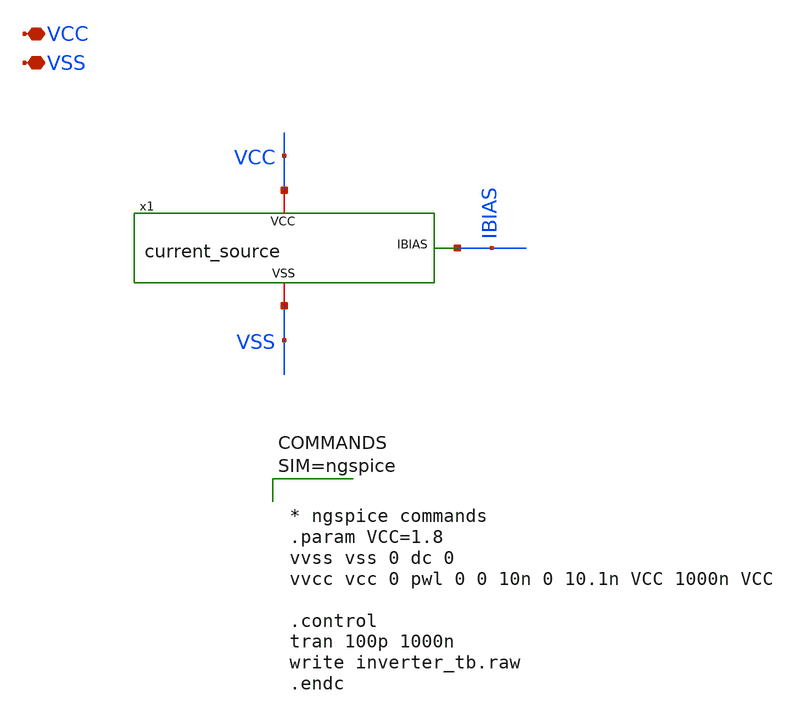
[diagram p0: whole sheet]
** sch_path: xschem/current_source_tb.sch
**.subckt current_source_tb VCC VSS
*.iopin VCC
*.iopin VSS
x1 VCC VSS IBIAS current_source
**** begin user architecture code

** opencircuitdesign pdks install
.lib $::SKYWATER_MODELS/sky130.lib.spice tt





* ngspice commands
.param VCC=1.8
vvss vss 0 dc 0
vvcc vcc 0 pwl 0 0 10n 0 10.1n VCC 1000n VCC

.control
tran 100p 1000n
write inverter_tb.raw
.endc




**** end user architecture code
**.ends

* expanding   symbol:  current_source.sym # of pins=3
** sym_path: xschem/current_source.sym
** sch_path: xschem/current_source.sch
.subckt current_source VCC VSS IBIAS
*.iopin VCC
*.iopin VSS
*.opin IBIAS
XM3 IBIAS IBIAS VSS VSS sky130_fd_pr__nfet_01v8 L=1 W=40 nf=1 ad='int((nf+1)/2) * W/nf * 0.29' as='int((nf+2)/2) * W/nf * 0.29'
+ pd='2*int((nf+1)/2) * (W/nf + 0.29)' ps='2*int((nf+2)/2) * (W/nf + 0.29)' nrd='0.29 / W' nrs='0.29 / W'
+ sa=0 sb=0 sd=0 mult=1 m=1
XR1 IBIAS VCC VSS sky130_fd_pr__res_xhigh_po W=1 L=9 mult=1 m=1
.ends

.end
